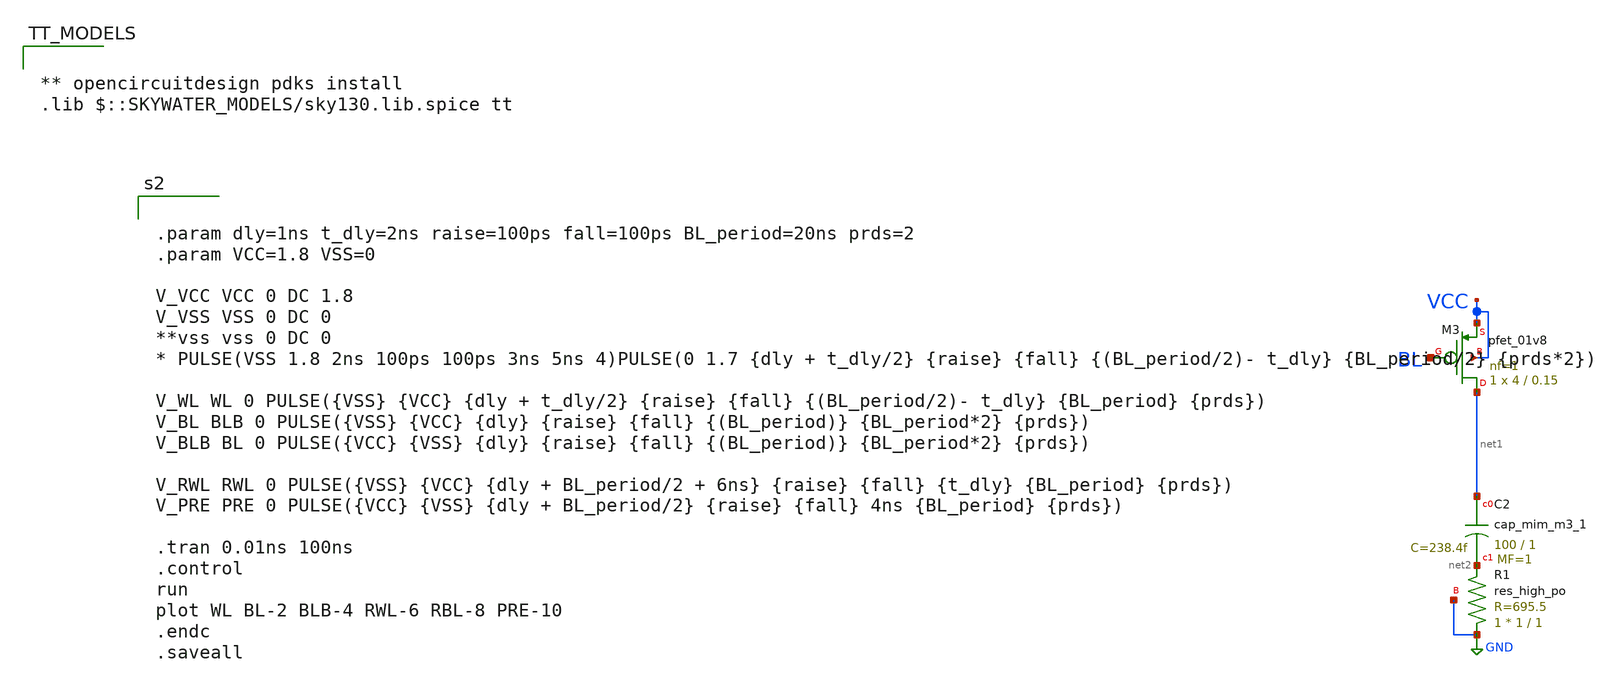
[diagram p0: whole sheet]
** sch_path: vscode/8T_sram_array_test - Copy - Copy.sch
**.subckt 8T_sram_array_test - Copy - Copy
XC2 net1 net2 sky130_fd_pr__cap_mim_m3_1 W=100 L=1 MF=1 m=1
XM3 net1 BL VCC VCC sky130_fd_pr__pfet_01v8 L=0.15 W=4 nf=1 ad='int((1 + 1)/2) * 4 / 1 * 0.29' as='int((1 + 2)/2) * 4 / 1 * 0.29'
+ pd='2*int((1 + 1)/2) * (4 / 1 + 0.29)' ps='2*int((1 + 2)/2) * (4 / 1 + 0.29)' nrd='0.29 / 4 ' nrs='0.29 / 4 '
+ sa=0 sb=0 sd=0 mult=1 m=1
XR1 GND net2 GND sky130_fd_pr__res_high_po W=1 L=1 mult=1 m=1
**** begin user architecture code


.param dly=1ns t_dly=2ns raise=100ps fall=100ps BL_period=20ns prds=2
.param VCC=1.8 VSS=0

V_VCC VCC 0 DC 1.8
V_VSS VSS 0 DC 0
**vss vss 0 DC 0
* PULSE(VSS 1.8 2ns 100ps 100ps 3ns 5ns 4)PULSE(0 1.7 {dly + t_dly/2} {raise} {fall} {(BL_period/2)- t_dly}
*+ {BL_period/2} {prds*2})

V_WL WL 0 PULSE({VSS} {VCC} {dly + t_dly/2} {raise} {fall} {(BL_period/2)- t_dly} {BL_period} {prds})
V_BL BLB 0 PULSE({VSS} {VCC} {dly} {raise} {fall} {(BL_period)} {BL_period*2} {prds})
V_BLB BL 0 PULSE({VCC} {VSS} {dly} {raise} {fall} {(BL_period)} {BL_period*2} {prds})

V_RWL RWL 0 PULSE({VSS} {VCC} {dly + BL_period/2 + 6ns} {raise} {fall} {t_dly} {BL_period} {prds})
V_PRE PRE 0 PULSE({VCC} {VSS} {dly + BL_period/2} {raise} {fall} 4ns {BL_period} {prds})

.tran 0.01ns 100ns
.control
run
plot WL BL-2 BLB-4 RWL-6 RBL-8 PRE-10
.endc
.saveall




** opencircuitdesign pdks install
.lib $::SKYWATER_MODELS/sky130.lib.spice tt

**** end user architecture code
**.ends
.GLOBAL GND
.end
